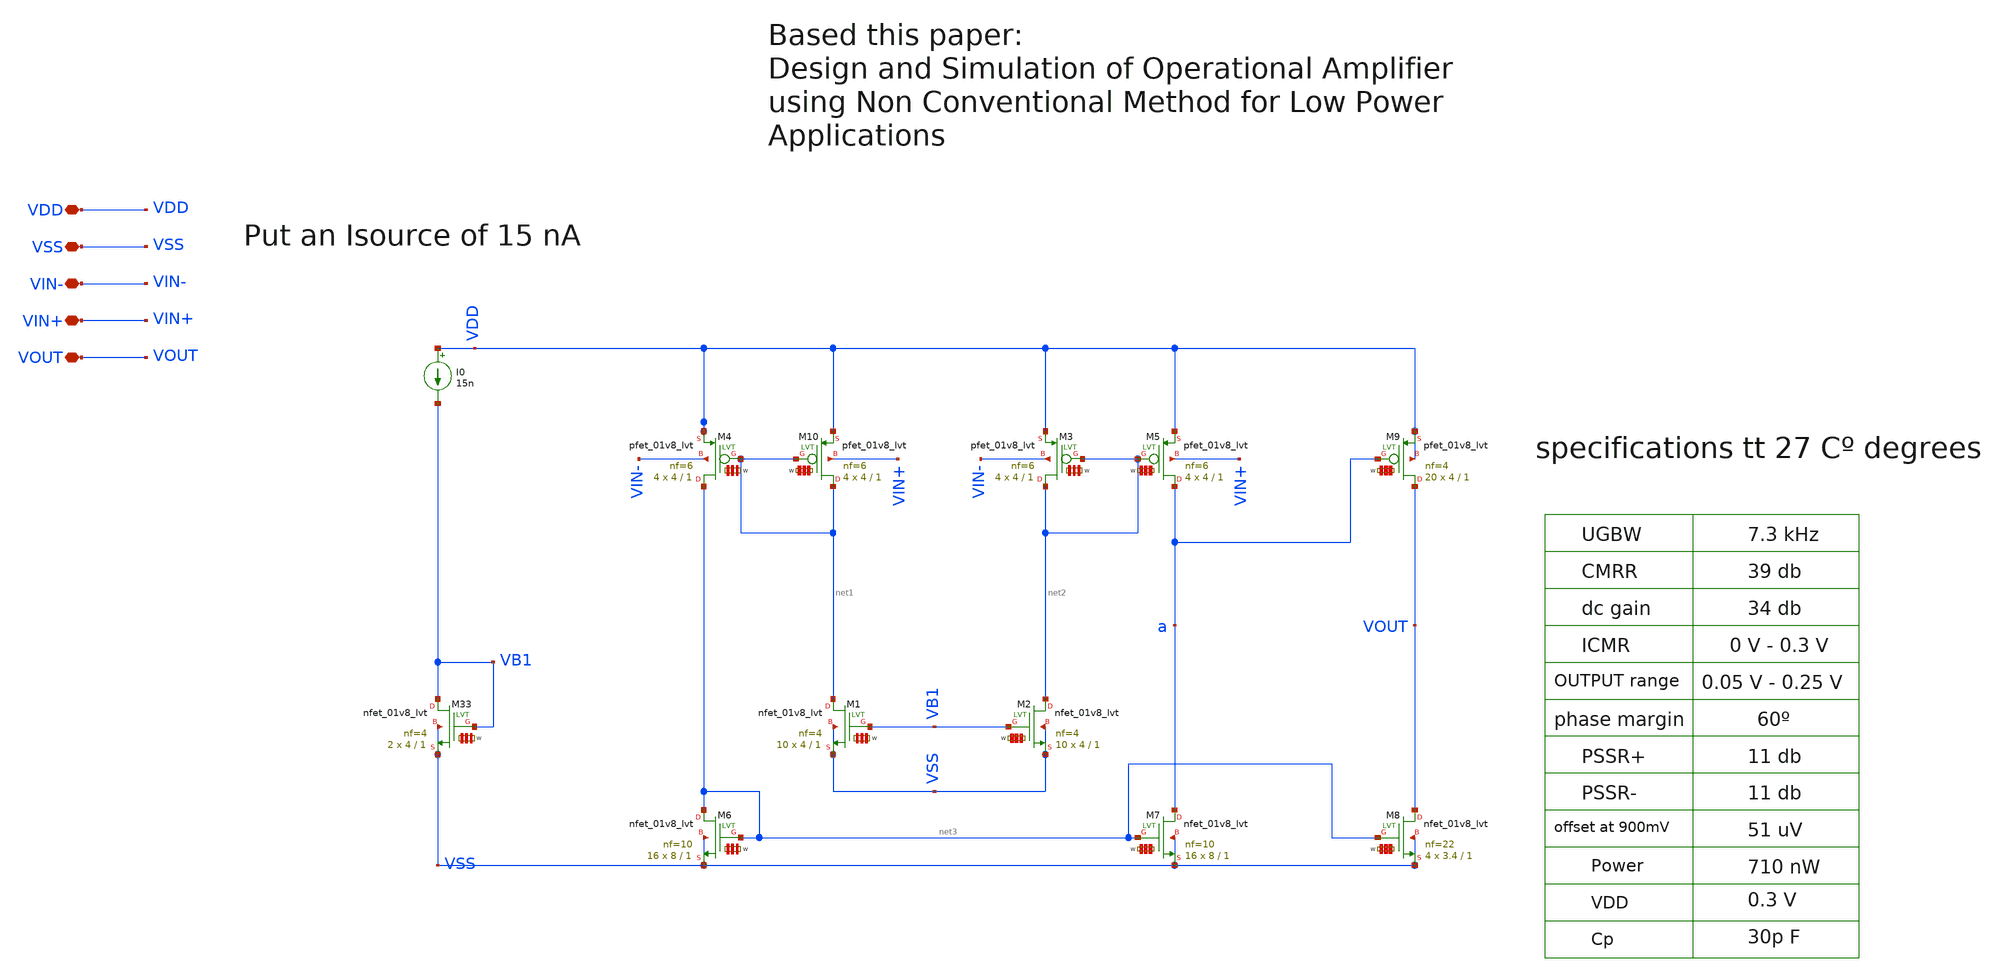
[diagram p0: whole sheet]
** sch_path: my_ip/LIB/LPA001_PMOS_0_3_sky130A.sch
**.subckt LPA001_PMOS_0_3_sky130A VDD VSS VIN- VIN+ VOUT
*.iopin VDD
*.iopin VSS
*.iopin VIN-
*.iopin VIN+
*.iopin VOUT
XM33 VB1 VB1 VSS VSS sky130_fd_pr__nfet_01v8_lvt L=1 W='4 * 4 ' nf=4 ad='int((4 + 1)/2) * 4 / 4 * 0.29'
+ as='int((4 + 2)/2) * 4 / 4 * 0.29' pd='2*int((4 + 1)/2) * (4 / 4 + 0.29)' ps='2*int((4 + 2)/2) * (4 / 4 + 0.29)'
+ nrd='0.29 / 4 ' nrs='0.29 / 4 ' sa=0 sb=0 sd=0 mult=2 m=2
XM1 net1 VB1 VSS VSS sky130_fd_pr__nfet_01v8_lvt L=1 W='4 * 4 ' nf=4 ad='int((4 + 1)/2) * 4 / 4 * 0.29'
+ as='int((4 + 2)/2) * 4 / 4 * 0.29' pd='2*int((4 + 1)/2) * (4 / 4 + 0.29)' ps='2*int((4 + 2)/2) * (4 / 4 + 0.29)'
+ nrd='0.29 / 4 ' nrs='0.29 / 4 ' sa=0 sb=0 sd=0 mult=10 m=10
XM2 net2 VB1 VSS VSS sky130_fd_pr__nfet_01v8_lvt L=1 W='4 * 4 ' nf=4 ad='int((4 + 1)/2) * 4 / 4 * 0.29'
+ as='int((4 + 2)/2) * 4 / 4 * 0.29' pd='2*int((4 + 1)/2) * (4 / 4 + 0.29)' ps='2*int((4 + 2)/2) * (4 / 4 + 0.29)'
+ nrd='0.29 / 4 ' nrs='0.29 / 4 ' sa=0 sb=0 sd=0 mult=10 m=10
XM5 a net2 VDD VIN+ sky130_fd_pr__pfet_01v8_lvt L=1 W='4 * 6 ' nf=6 ad='int((6 + 1)/2) * 4 / 6 * 0.29'
+ as='int((6 + 2)/2) * 4 / 6 * 0.29' pd='2*int((6 + 1)/2) * (4 / 6 + 0.29)' ps='2*int((6 + 2)/2) * (4 / 6 + 0.29)'
+ nrd='0.29 / 4 ' nrs='0.29 / 4 ' sa=0 sb=0 sd=0 mult=4 m=4
XM6 net3 net3 VSS VSS sky130_fd_pr__nfet_01v8_lvt L=1 W='8 * 10 ' nf=10 ad='int((10 + 1)/2) * 8 / 10 * 0.29'
+ as='int((10 + 2)/2) * 8 / 10 * 0.29' pd='2*int((10 + 1)/2) * (8 / 10 + 0.29)' ps='2*int((10 + 2)/2) * (8 / 10 + 0.29)'
+ nrd='0.29 / 8 ' nrs='0.29 / 8 ' sa=0 sb=0 sd=0 mult=16 m=16
XM7 a net3 VSS VSS sky130_fd_pr__nfet_01v8_lvt L=1 W='8 * 10 ' nf=10 ad='int((10 + 1)/2) * 8 / 10 * 0.29'
+ as='int((10 + 2)/2) * 8 / 10 * 0.29' pd='2*int((10 + 1)/2) * (8 / 10 + 0.29)' ps='2*int((10 + 2)/2) * (8 / 10 + 0.29)'
+ nrd='0.29 / 8 ' nrs='0.29 / 8 ' sa=0 sb=0 sd=0 mult=16 m=16
XM8 VOUT net3 VSS VSS sky130_fd_pr__nfet_01v8_lvt L=1 W='3.4 * 22 ' nf=22 ad='int((22 + 1)/2) * 3.4 / 22 * 0.29'
+ as='int((22 + 2)/2) * 3.4 / 22 * 0.29' pd='2*int((22 + 1)/2) * (3.4 / 22 + 0.29)' ps='2*int((22 + 2)/2) * (3.4 / 22 + 0.29)'
+ nrd='0.29 / 3.4 ' nrs='0.29 / 3.4 ' sa=0 sb=0 sd=0 mult=4 m=4
XM9 VOUT a VDD VDD sky130_fd_pr__pfet_01v8_lvt L=1 W='4 * 4 ' nf=4 ad='int((4 + 1)/2) * 4 / 4 * 0.29'
+ as='int((4 + 2)/2) * 4 / 4 * 0.29' pd='2*int((4 + 1)/2) * (4 / 4 + 0.29)' ps='2*int((4 + 2)/2) * (4 / 4 + 0.29)'
+ nrd='0.29 / 4 ' nrs='0.29 / 4 ' sa=0 sb=0 sd=0 mult=20 m=20
XM3 net2 net2 VDD VIN- sky130_fd_pr__pfet_01v8_lvt L=1 W='4 * 6 ' nf=6 ad='int((6 + 1)/2) * 4 / 6 * 0.29'
+ as='int((6 + 2)/2) * 4 / 6 * 0.29' pd='2*int((6 + 1)/2) * (4 / 6 + 0.29)' ps='2*int((6 + 2)/2) * (4 / 6 + 0.29)'
+ nrd='0.29 / 4 ' nrs='0.29 / 4 ' sa=0 sb=0 sd=0 mult=4 m=4
XM4 net3 net1 VDD VIN- sky130_fd_pr__pfet_01v8_lvt L=1 W='4 * 6 ' nf=6 ad='int((6 + 1)/2) * 4 / 6 * 0.29'
+ as='int((6 + 2)/2) * 4 / 6 * 0.29' pd='2*int((6 + 1)/2) * (4 / 6 + 0.29)' ps='2*int((6 + 2)/2) * (4 / 6 + 0.29)'
+ nrd='0.29 / 4 ' nrs='0.29 / 4 ' sa=0 sb=0 sd=0 mult=4 m=4
XM10 net1 net1 VDD VIN+ sky130_fd_pr__pfet_01v8_lvt L=1 W='4 * 6 ' nf=6 ad='int((6 + 1)/2) * 4 / 6 * 0.29'
+ as='int((6 + 2)/2) * 4 / 6 * 0.29' pd='2*int((6 + 1)/2) * (4 / 6 + 0.29)' ps='2*int((6 + 2)/2) * (4 / 6 + 0.29)'
+ nrd='0.29 / 4 ' nrs='0.29 / 4 ' sa=0 sb=0 sd=0 mult=4 m=4
I0 VDD VB1 15n
**.ends
.end
